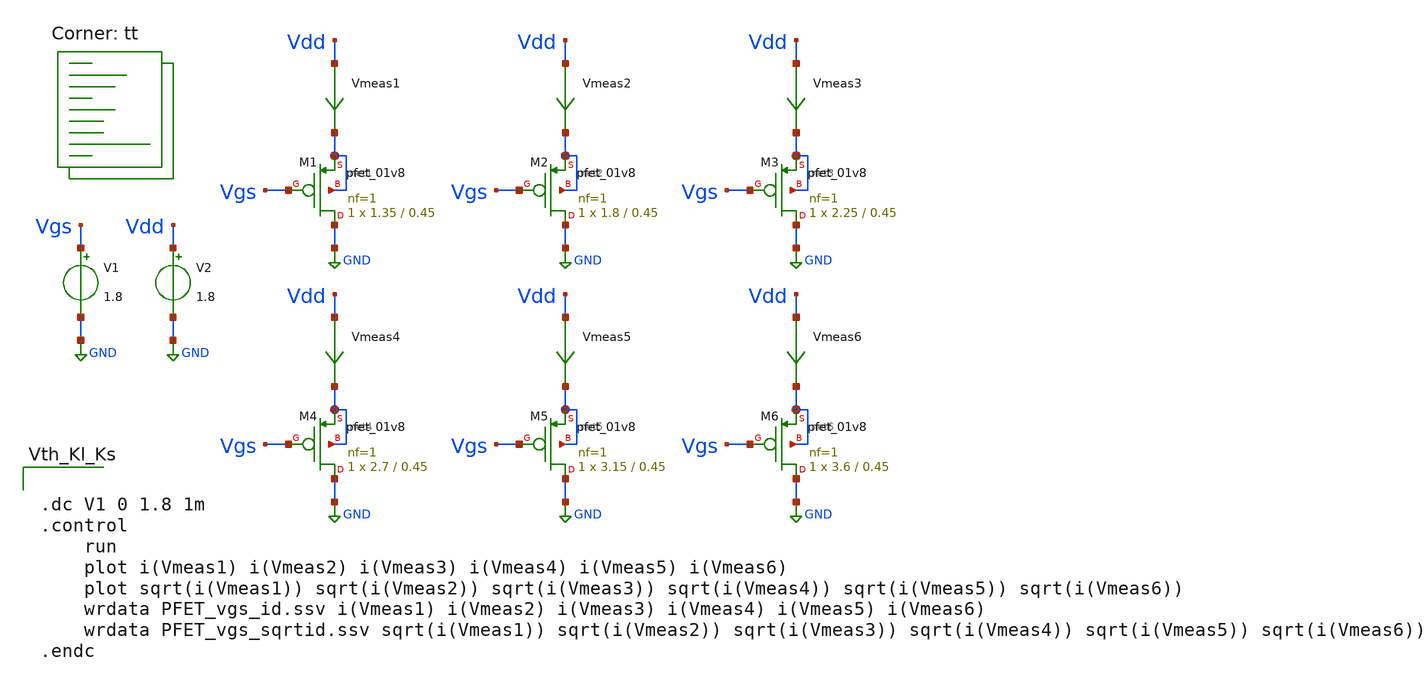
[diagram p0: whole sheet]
** sch_path: opamp_design/Parametros_cmos/PFET_param1.sch
**.subckt PFET_param1
Vmeas1 Vdd net1 0
.save i(vmeas1)
V2 Vdd GND 1.8
V1 Vgs GND 1.8
Vmeas2 Vdd net2 0
.save i(vmeas2)
Vmeas3 Vdd net3 0
.save i(vmeas3)
Vmeas4 Vdd net4 0
.save i(vmeas4)
Vmeas5 Vdd net5 0
.save i(vmeas5)
Vmeas6 Vdd net6 0
.save i(vmeas6)
XM1 GND Vgs net1 net1 sky130_fd_pr__pfet_01v8 L=0.45 W=1.35 nf=1 ad='int((nf+1)/2) * W/nf * 0.29' as='int((nf+2)/2) * W/nf * 0.29'
+ pd='2*int((nf+1)/2) * (W/nf + 0.29)' ps='2*int((nf+2)/2) * (W/nf + 0.29)' nrd='0.29 / W' nrs='0.29 / W'
+ sa=0 sb=0 sd=0 mult=1 m=1
XM2 GND Vgs net2 net2 sky130_fd_pr__pfet_01v8 L=0.45 W=1.8 nf=1 ad='int((nf+1)/2) * W/nf * 0.29' as='int((nf+2)/2) * W/nf * 0.29'
+ pd='2*int((nf+1)/2) * (W/nf + 0.29)' ps='2*int((nf+2)/2) * (W/nf + 0.29)' nrd='0.29 / W' nrs='0.29 / W'
+ sa=0 sb=0 sd=0 mult=1 m=1
XM3 GND Vgs net3 net3 sky130_fd_pr__pfet_01v8 L=0.45 W=2.25 nf=1 ad='int((nf+1)/2) * W/nf * 0.29' as='int((nf+2)/2) * W/nf * 0.29'
+ pd='2*int((nf+1)/2) * (W/nf + 0.29)' ps='2*int((nf+2)/2) * (W/nf + 0.29)' nrd='0.29 / W' nrs='0.29 / W'
+ sa=0 sb=0 sd=0 mult=1 m=1
XM4 GND Vgs net4 net4 sky130_fd_pr__pfet_01v8 L=0.45 W=2.7 nf=1 ad='int((nf+1)/2) * W/nf * 0.29' as='int((nf+2)/2) * W/nf * 0.29'
+ pd='2*int((nf+1)/2) * (W/nf + 0.29)' ps='2*int((nf+2)/2) * (W/nf + 0.29)' nrd='0.29 / W' nrs='0.29 / W'
+ sa=0 sb=0 sd=0 mult=1 m=1
XM5 GND Vgs net5 net5 sky130_fd_pr__pfet_01v8 L=0.45 W=3.15 nf=1 ad='int((nf+1)/2) * W/nf * 0.29' as='int((nf+2)/2) * W/nf * 0.29'
+ pd='2*int((nf+1)/2) * (W/nf + 0.29)' ps='2*int((nf+2)/2) * (W/nf + 0.29)' nrd='0.29 / W' nrs='0.29 / W'
+ sa=0 sb=0 sd=0 mult=1 m=1
XM6 GND Vgs net6 net6 sky130_fd_pr__pfet_01v8 L=0.45 W=3.6 nf=1 ad='int((nf+1)/2) * W/nf * 0.29' as='int((nf+2)/2) * W/nf * 0.29'
+ pd='2*int((nf+1)/2) * (W/nf + 0.29)' ps='2*int((nf+2)/2) * (W/nf + 0.29)' nrd='0.29 / W' nrs='0.29 / W'
+ sa=0 sb=0 sd=0 mult=1 m=1
**** begin user architecture code
.lib $::SKYWATER_MODELS/sky130.lib.spice tt


.dc V1 0 1.8 1m
.control
	run
	plot i(Vmeas1) i(Vmeas2) i(Vmeas3) i(Vmeas4) i(Vmeas5) i(Vmeas6)
	plot sqrt(i(Vmeas1)) sqrt(i(Vmeas2)) sqrt(i(Vmeas3)) sqrt(i(Vmeas4)) sqrt(i(Vmeas5))
+ sqrt(i(Vmeas6))
	wrdata PFET_vgs_id.ssv i(Vmeas1) i(Vmeas2) i(Vmeas3) i(Vmeas4) i(Vmeas5) i(Vmeas6)
	wrdata PFET_vgs_sqrtid.ssv sqrt(i(Vmeas1)) sqrt(i(Vmeas2)) sqrt(i(Vmeas3)) sqrt(i(Vmeas4))
+ sqrt(i(Vmeas5)) sqrt(i(Vmeas6))
.endc


**** end user architecture code
**.ends
.GLOBAL GND
.end
